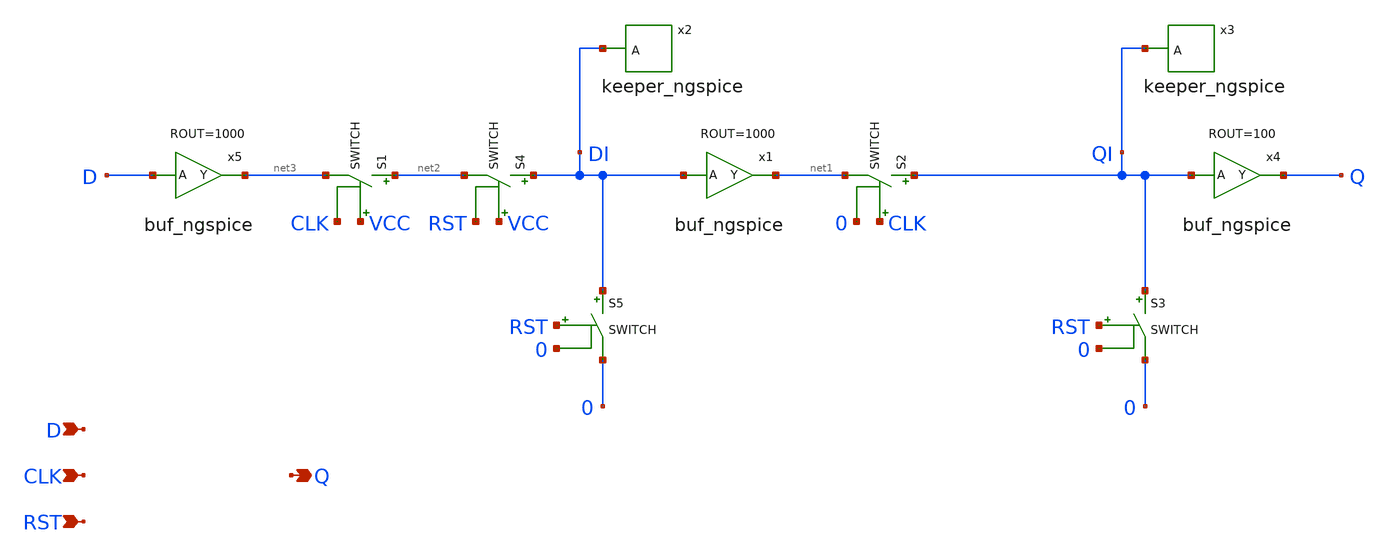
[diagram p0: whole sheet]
** sch_path: xschem_library/ngspice/flip_flop_ngspice.sch
* Copyright (C) 1998-2023 Stefan Frederik Schippers
* This program is free software; you can redistribute it and/or modify
* it under the terms of the GNU General Public License as published by
* the Free Software Foundation; either version 2 of the License, or
* (at your option) any later version.
* This program is distributed in the hope that it will be useful,
* but WITHOUT ANY WARRANTY; without even the implied warranty of
* MERCHANTABILITY or FITNESS FOR A PARTICULAR PURPOSE.  See the
* GNU General Public License for more details.
* You should have received a copy of the GNU General Public License
* along with this program; if not, write to the Free Software
**.subckt flip_flop_ngspice D CLK RST Q
*.ipin D
*.ipin CLK
*.ipin RST
*.opin Q
x2 DI keeper_ngspice
S1 net2 net3 VCC CLK SWITCH
S2 QI net1 CLK 0 SWITCH
x3 QI keeper_ngspice
x4 Q QI buf_ngspice ROUT=100
S3 QI 0 RST 0 SWITCH
x1 net1 DI buf_ngspice ROUT=1000
S4 DI net2 VCC RST SWITCH
S5 DI 0 RST 0 SWITCH
x5 net3 D buf_ngspice ROUT=1000
**.ends

* expanding   symbol:  keeper_ngspice.sym # of pins=1
** sym_path: xschem_library/ngspice/keeper_ngspice.sym
** sch_path: xschem_library/ngspice/keeper_ngspice.sch
.subckt keeper_ngspice A
*.ipin A
x1 Y A inv_ngspice ROUT=1000
x2 A Y inv_ngspice ROUT=300k
.ends


* expanding   symbol:  buf_ngspice.sym # of pins=2
** sym_path: xschem_library/ngspice/buf_ngspice.sym
** sch_path: xschem_library/ngspice/buf_ngspice.sch
.subckt buf_ngspice Y A  ROUT=1000
*.ipin A
*.opin Y
B1 net1 0 V = 'VCC/2*(1+tanh((V(A1)-VCC/2)*100))'
R1 Y1 net1 'ROUT' m=1
C3 Y1 0 8f m=1
C1 A1 0 4f m=1
V1 Y Y1 0
V2 A1 A 0
.ends


* expanding   symbol:  inv_ngspice.sym # of pins=2
** sym_path: xschem_library/ngspice/inv_ngspice.sym
** sch_path: xschem_library/ngspice/inv_ngspice.sch
.subckt inv_ngspice Y A  ROUT=1000
*.ipin A
*.opin Y
B1 net1 0 V = 'VCC/2*(1-tanh((V(A1)-VCC/2)*100))'
R1 Y1 net1 'ROUT' m=1
C1 A1 0 8f m=1
C2 Y1 0 8f m=1
V1 Y Y1 0
.save i(v1)
V2 A1 A 0
.save i(v2)
.ends

.end
